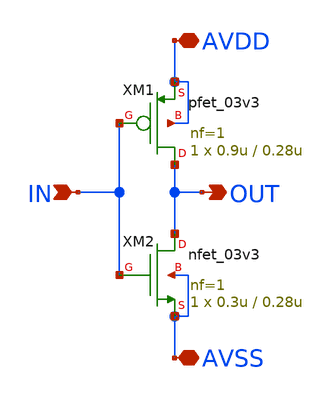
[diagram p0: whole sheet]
** sch_path: designs/libs/core_analog/inv/inv.sch
**.subckt inv IN AVDD AVSS OUT
*.ipin IN
*.iopin AVDD
*.iopin AVSS
*.opin OUT
XM1 OUT IN AVDD AVDD pfet_03v3 L=0.28u W=0.9u nf=1 ad='int((nf+1)/2) * W/nf * 0.18u' as='int((nf+2)/2) * W/nf * 0.18u'
+ pd='2*int((nf+1)/2) * (W/nf + 0.18u)' ps='2*int((nf+2)/2) * (W/nf + 0.18u)' nrd='0.18u / W' nrs='0.18u / W'
+ sa=0 sb=0 sd=0 m=1
XM2 OUT IN AVSS AVSS nfet_03v3 L=0.28u W=0.3u nf=1 ad='int((nf+1)/2) * W/nf * 0.18u' as='int((nf+2)/2) * W/nf * 0.18u'
+ pd='2*int((nf+1)/2) * (W/nf + 0.18u)' ps='2*int((nf+2)/2) * (W/nf + 0.18u)' nrd='0.18u / W' nrs='0.18u / W'
+ sa=0 sb=0 sd=0 m=1
**.ends
.end
